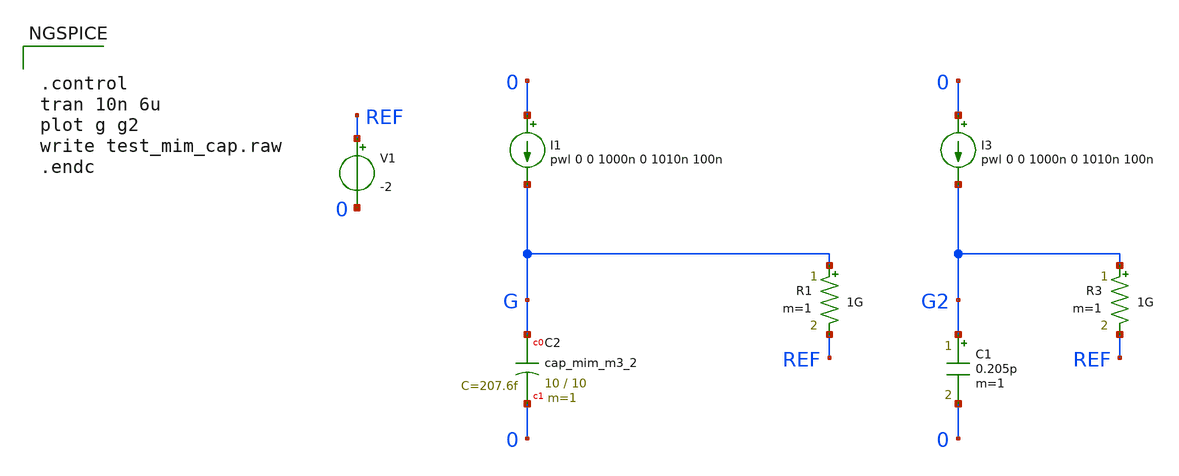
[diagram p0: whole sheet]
** sch_path: sky130_tests/test_mim_cap.sch
* Copyright 2021 Stefan Frederik Schippers
* Licensed under the Apache License, Version 2.0 (the "License");
* you may not use this file except in compliance with the License.
* You may obtain a copy of the License at
* https://www.apache.org/licenses/LICENSE-2.0
* Unless required by applicable law or agreed to in writing, software
* distributed under the License is distributed on an "AS IS" BASIS,
* WITHOUT WARRANTIES OR CONDITIONS OF ANY KIND, either express or implied.
* See the License for the specific language governing permissions and
* limitations under the License.
**.subckt test_mim_cap
I1 0 G pwl 0 0 1000n 0 1010n 100n
R1 G REF 1G m=1
I3 0 G2 pwl 0 0 1000n 0 1010n 100n
R3 G2 REF 1G m=1
C1 G2 0 0.205p m=1
V1 REF 0 -2
XC2 G 0 sky130_fd_pr__cap_mim_m3_2 W=10 L=10 MF=1 m=1
**** begin user architecture code


.control
tran 10n 6u
plot g g2
write test_mim_cap.raw
.endc


 ** manual skywater pdks install (with patches applied)
* .lib $::SKYWATER_MODELS/models/sky130.lib.spice tt

** opencircuitdesign pdks install
.lib $::SKYWATER_MODELS/sky130.lib.spice tt

.param mc_mm_switch=0
.param mc_pr_switch=0

**** end user architecture code
**.ends
.end
